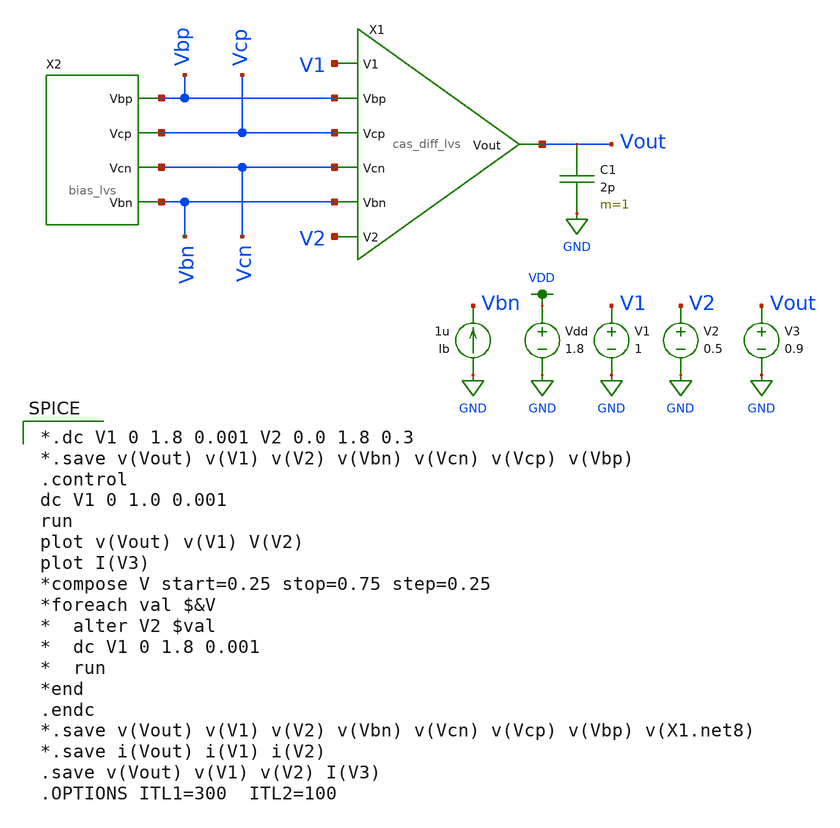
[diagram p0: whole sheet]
** sch_path: mini3/schem/v2itc_noninv.sch
**.subckt v2itc_noninv
X1 V1 V2 Vout Vbp Vcp Vcn Vbn cas_diff_lvs
Vdd VDD GND 1.8
V1 V1 GND 1
V2 V2 GND 0.5
Ib GND Vbn 1u
C1 Vout GND 2p m=1
X2 Vbp Vcp Vcn Vbn bias_lvs
V3 Vout GND 0.9
**** begin user architecture code

.option wnflag=1
.lib ~/skywater/skywater-pdk/libraries/sky130_fd_pr_ngspice/latest/models/sky130.lib.spice tt


*.dc V1 0 1.8 0.001 V2 0.0 1.8 0.3
*.save v(Vout) v(V1) v(V2) v(Vbn) v(Vcn) v(Vcp) v(Vbp)
.control
dc V1 0 1.0 0.001
run
plot v(Vout) v(V1) V(V2)
plot I(V3)
*compose V start=0.25 stop=0.75 step=0.25
*foreach val $&V
*  alter V2 $val
*  dc V1 0 1.8 0.001
*  run
*end
.endc
*.save v(Vout) v(V1) v(V2) v(Vbn) v(Vcn) v(Vcp) v(Vbp) v(X1.net8)
*.save i(Vout) i(V1) i(V2)
.save v(Vout) v(V1) v(V2) I(V3)
.OPTIONS ITL1=300  ITL2=100

**** end user architecture code
**.ends
.GLOBAL VDD
.GLOBAL GND
.end
